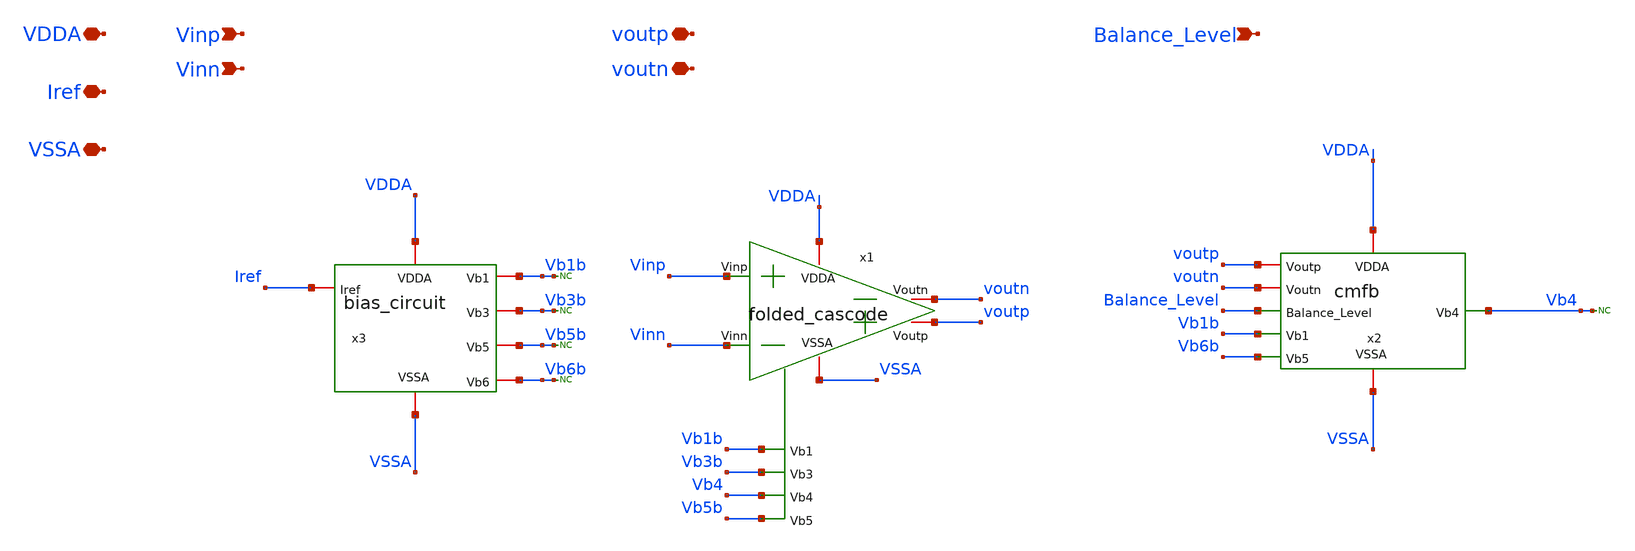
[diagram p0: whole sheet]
** sch_path: Folded_cascode/schematic/top_fc.sch
**.subckt top_fc Iref VDDA VSSA Vinp Vinn Balance_Level voutp voutn
*.iopin Iref
*.iopin VDDA
*.iopin VSSA
*.ipin Vinp
*.ipin Vinn
*.ipin Balance_Level
*.iopin voutp
*.iopin voutn
x2 VDDA VSSA voutp voutn Balance_Level Vb1b Vb4 Vb6b cmfb
* noconn Vb3b
* noconn Vb5b
* noconn Vb1b
* noconn Vb6b
x3 VDDA Vb3b Vb1b Vb5b VSSA Iref Vb6b bias_circuit
* noconn Vb4
x1 VDDA VSSA Vinp Vinn voutp voutn Vb1b Vb3b Vb4 Vb5b folded_cascode
**.ends
.end
